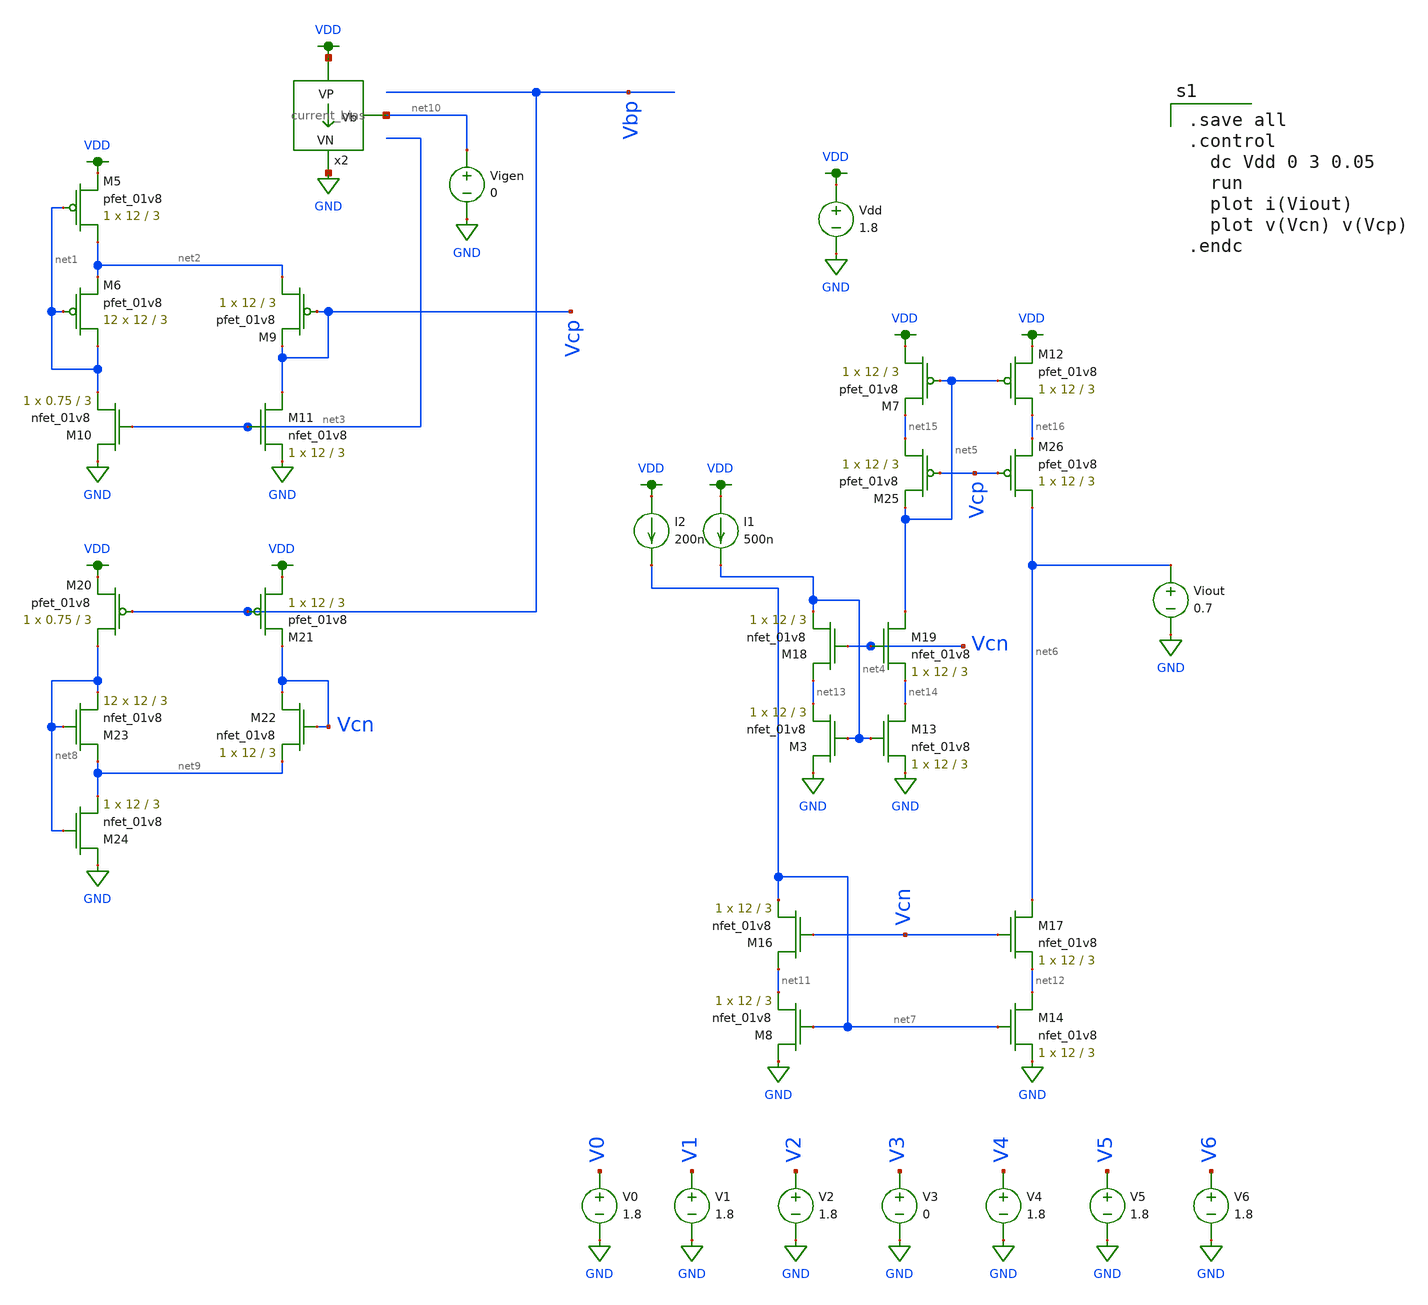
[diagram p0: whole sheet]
** sch_path: schematics/ieee DAC/ieee_DAC_mc_simulation_5.sch
**.subckt ieee_DAC_mc_simulation_5
Vdd VDD GND 1.8
V1 V1 GND 1.8
V2 V2 GND 1.8
V3 V3 GND 0
V4 V4 GND 1.8
V5 V5 GND 1.8
V6 V6 GND 1.8
V0 V0 GND 1.8
XM5 net2 net1 VDD VDD sky130_fd_pr__pfet_01v8 L=3 W=12 nf=1 ad='int((nf+1)/2) * W/nf * 0.29' as='int((nf+2)/2) * W/nf * 0.29'
+ pd='2*int((nf+1)/2) * (W/nf + 0.29)' ps='2*int((nf+2)/2) * (W/nf + 0.29)' nrd='0.29 / W' nrs='0.29 / W'
+ sa=0 sb=0 sd=0 mult=1 m=1
XM6 net1 net1 net2 VDD sky130_fd_pr__pfet_01v8 L=3 W=12 nf=1 ad='int((nf+1)/2) * W/nf * 0.29' as='int((nf+2)/2) * W/nf * 0.29'
+ pd='2*int((nf+1)/2) * (W/nf + 0.29)' ps='2*int((nf+2)/2) * (W/nf + 0.29)' nrd='0.29 / W' nrs='0.29 / W'
+ sa=0 sb=0 sd=0 mult=12 m=12
XM9 net2 Vcp Vcp VDD sky130_fd_pr__pfet_01v8 L=3 W=12 nf=1 ad='int((nf+1)/2) * W/nf * 0.29' as='int((nf+2)/2) * W/nf * 0.29'
+ pd='2*int((nf+1)/2) * (W/nf + 0.29)' ps='2*int((nf+2)/2) * (W/nf + 0.29)' nrd='0.29 / W' nrs='0.29 / W'
+ sa=0 sb=0 sd=0 mult=1 m=1
XM10 GND net3 net1 GND sky130_fd_pr__nfet_01v8 L=3 W=0.75 nf=1 ad='int((nf+1)/2) * W/nf * 0.29' as='int((nf+2)/2) * W/nf * 0.29'
+ pd='2*int((nf+1)/2) * (W/nf + 0.29)' ps='2*int((nf+2)/2) * (W/nf + 0.29)' nrd='0.29 / W' nrs='0.29 / W'
+ sa=0 sb=0 sd=0 mult=1 m=1
XM11 Vcp net3 GND GND sky130_fd_pr__nfet_01v8 L=3 W=12 nf=1 ad='int((nf+1)/2) * W/nf * 0.29' as='int((nf+2)/2) * W/nf * 0.29'
+ pd='2*int((nf+1)/2) * (W/nf + 0.29)' ps='2*int((nf+2)/2) * (W/nf + 0.29)' nrd='0.29 / W' nrs='0.29 / W'
+ sa=0 sb=0 sd=0 mult=1 m=1
x2 VDD net10 GND current_bias
Vigen net10 GND 0
XM3 GND net4 net13 GND sky130_fd_pr__nfet_01v8 L=3 W=12 nf=1 ad='int((nf+1)/2) * W/nf * 0.29' as='int((nf+2)/2) * W/nf * 0.29'
+ pd='2*int((nf+1)/2) * (W/nf + 0.29)' ps='2*int((nf+2)/2) * (W/nf + 0.29)' nrd='0.29 / W' nrs='0.29 / W'
+ sa=0 sb=0 sd=0 mult=1 m=1
XM7 VDD net5 net15 VDD sky130_fd_pr__pfet_01v8 L=3 W=12 nf=1 ad='int((nf+1)/2) * W/nf * 0.29' as='int((nf+2)/2) * W/nf * 0.29'
+ pd='2*int((nf+1)/2) * (W/nf + 0.29)' ps='2*int((nf+2)/2) * (W/nf + 0.29)' nrd='0.29 / W' nrs='0.29 / W'
+ sa=0 sb=0 sd=0 mult=1 m=1
XM8 GND net7 net11 GND sky130_fd_pr__nfet_01v8 L=3 W=12 nf=1 ad='int((nf+1)/2) * W/nf * 0.29' as='int((nf+2)/2) * W/nf * 0.29'
+ pd='2*int((nf+1)/2) * (W/nf + 0.29)' ps='2*int((nf+2)/2) * (W/nf + 0.29)' nrd='0.29 / W' nrs='0.29 / W'
+ sa=0 sb=0 sd=0 mult=1 m=1
XM12 net16 net5 VDD VDD sky130_fd_pr__pfet_01v8 L=3 W=12 nf=1 ad='int((nf+1)/2) * W/nf * 0.29' as='int((nf+2)/2) * W/nf * 0.29'
+ pd='2*int((nf+1)/2) * (W/nf + 0.29)' ps='2*int((nf+2)/2) * (W/nf + 0.29)' nrd='0.29 / W' nrs='0.29 / W'
+ sa=0 sb=0 sd=0 mult=1 m=1
Viout net6 GND 0.7
XM13 net14 net4 GND GND sky130_fd_pr__nfet_01v8 L=3 W=12 nf=1 ad='int((nf+1)/2) * W/nf * 0.29' as='int((nf+2)/2) * W/nf * 0.29'
+ pd='2*int((nf+1)/2) * (W/nf + 0.29)' ps='2*int((nf+2)/2) * (W/nf + 0.29)' nrd='0.29 / W' nrs='0.29 / W'
+ sa=0 sb=0 sd=0 mult=1 m=1
XM14 net12 net7 GND GND sky130_fd_pr__nfet_01v8 L=3 W=12 nf=1 ad='int((nf+1)/2) * W/nf * 0.29' as='int((nf+2)/2) * W/nf * 0.29'
+ pd='2*int((nf+1)/2) * (W/nf + 0.29)' ps='2*int((nf+2)/2) * (W/nf + 0.29)' nrd='0.29 / W' nrs='0.29 / W'
+ sa=0 sb=0 sd=0 mult=1 m=1
XM20 net8 Vbp VDD VDD sky130_fd_pr__pfet_01v8 L=3 W=0.75 nf=1 ad='int((nf+1)/2) * W/nf * 0.29' as='int((nf+2)/2) * W/nf * 0.29'
+ pd='2*int((nf+1)/2) * (W/nf + 0.29)' ps='2*int((nf+2)/2) * (W/nf + 0.29)' nrd='0.29 / W' nrs='0.29 / W'
+ sa=0 sb=0 sd=0 mult=1 m=1
XM21 VDD Vbp Vcn VDD sky130_fd_pr__pfet_01v8 L=3 W=12 nf=1 ad='int((nf+1)/2) * W/nf * 0.29' as='int((nf+2)/2) * W/nf * 0.29'
+ pd='2*int((nf+1)/2) * (W/nf + 0.29)' ps='2*int((nf+2)/2) * (W/nf + 0.29)' nrd='0.29 / W' nrs='0.29 / W'
+ sa=0 sb=0 sd=0 mult=1 m=1
XM22 Vcn Vcn net9 GND sky130_fd_pr__nfet_01v8 L=3 W=12 nf=1 ad='int((nf+1)/2) * W/nf * 0.29' as='int((nf+2)/2) * W/nf * 0.29'
+ pd='2*int((nf+1)/2) * (W/nf + 0.29)' ps='2*int((nf+2)/2) * (W/nf + 0.29)' nrd='0.29 / W' nrs='0.29 / W'
+ sa=0 sb=0 sd=0 mult=1 m=1
XM23 net9 net8 net8 GND sky130_fd_pr__nfet_01v8 L=3 W=12 nf=1 ad='int((nf+1)/2) * W/nf * 0.29' as='int((nf+2)/2) * W/nf * 0.29'
+ pd='2*int((nf+1)/2) * (W/nf + 0.29)' ps='2*int((nf+2)/2) * (W/nf + 0.29)' nrd='0.29 / W' nrs='0.29 / W'
+ sa=0 sb=0 sd=0 mult=12 m=12
XM24 GND net8 net9 GND sky130_fd_pr__nfet_01v8 L=3 W=12 nf=1 ad='int((nf+1)/2) * W/nf * 0.29' as='int((nf+2)/2) * W/nf * 0.29'
+ pd='2*int((nf+1)/2) * (W/nf + 0.29)' ps='2*int((nf+2)/2) * (W/nf + 0.29)' nrd='0.29 / W' nrs='0.29 / W'
+ sa=0 sb=0 sd=0 mult=1 m=1
XM16 net11 Vcn net7 GND sky130_fd_pr__nfet_01v8 L=3 W=12 nf=1 ad='int((nf+1)/2) * W/nf * 0.29' as='int((nf+2)/2) * W/nf * 0.29'
+ pd='2*int((nf+1)/2) * (W/nf + 0.29)' ps='2*int((nf+2)/2) * (W/nf + 0.29)' nrd='0.29 / W' nrs='0.29 / W'
+ sa=0 sb=0 sd=0 mult=1 m=1
XM17 net6 Vcn net12 GND sky130_fd_pr__nfet_01v8 L=3 W=12 nf=1 ad='int((nf+1)/2) * W/nf * 0.29' as='int((nf+2)/2) * W/nf * 0.29'
+ pd='2*int((nf+1)/2) * (W/nf + 0.29)' ps='2*int((nf+2)/2) * (W/nf + 0.29)' nrd='0.29 / W' nrs='0.29 / W'
+ sa=0 sb=0 sd=0 mult=1 m=1
XM18 net13 Vcn net4 GND sky130_fd_pr__nfet_01v8 L=3 W=12 nf=1 ad='int((nf+1)/2) * W/nf * 0.29' as='int((nf+2)/2) * W/nf * 0.29'
+ pd='2*int((nf+1)/2) * (W/nf + 0.29)' ps='2*int((nf+2)/2) * (W/nf + 0.29)' nrd='0.29 / W' nrs='0.29 / W'
+ sa=0 sb=0 sd=0 mult=1 m=1
XM19 net5 Vcn net14 GND sky130_fd_pr__nfet_01v8 L=3 W=12 nf=1 ad='int((nf+1)/2) * W/nf * 0.29' as='int((nf+2)/2) * W/nf * 0.29'
+ pd='2*int((nf+1)/2) * (W/nf + 0.29)' ps='2*int((nf+2)/2) * (W/nf + 0.29)' nrd='0.29 / W' nrs='0.29 / W'
+ sa=0 sb=0 sd=0 mult=1 m=1
XM25 net15 Vcp net5 VDD sky130_fd_pr__pfet_01v8 L=3 W=12 nf=1 ad='int((nf+1)/2) * W/nf * 0.29' as='int((nf+2)/2) * W/nf * 0.29'
+ pd='2*int((nf+1)/2) * (W/nf + 0.29)' ps='2*int((nf+2)/2) * (W/nf + 0.29)' nrd='0.29 / W' nrs='0.29 / W'
+ sa=0 sb=0 sd=0 mult=1 m=1
XM26 net6 Vcp net16 VDD sky130_fd_pr__pfet_01v8 L=3 W=12 nf=1 ad='int((nf+1)/2) * W/nf * 0.29' as='int((nf+2)/2) * W/nf * 0.29'
+ pd='2*int((nf+1)/2) * (W/nf + 0.29)' ps='2*int((nf+2)/2) * (W/nf + 0.29)' nrd='0.29 / W' nrs='0.29 / W'
+ sa=0 sb=0 sd=0 mult=1 m=1
I1 VDD net4 500n
I2 VDD net7 200n
**** begin user architecture code

.option wnflag=1
.param MC_SWITCH=1.0
.lib ~/skywater/skywater-pdk/libraries/sky130_fd_pr_ngspice/latest/models/sky130.lib.spice tt


.save all
.control
  dc Vdd 0 3 0.05
  run
  plot i(Viout)
  plot v(Vcn) v(Vcp)
.endc

**** end user architecture code
**.ends
.GLOBAL VDD
.GLOBAL GND
.end
